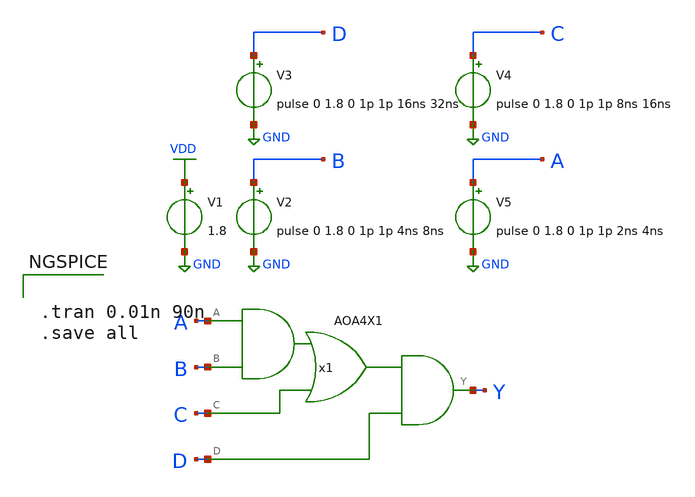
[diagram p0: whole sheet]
** sch_path: current/xschem/test_AOA4X1.sch
**.subckt test_AOA4X1
V2 B GND pulse 0 1.8 0 1p 1p 4ns 8ns
V1 VDD GND 1.8
V3 D GND pulse 0 1.8 0 1p 1p 16ns 32ns
V4 C GND pulse 0 1.8 0 1p 1p 8ns 16ns
V5 A GND pulse 0 1.8 0 1p 1p 2ns 4ns
x1 Y A B C D VDD GND AOA4X1
**** begin user architecture code

.lib $::SKYWATER_MODELS/sky130.lib.spice tt


**** end user architecture code
**.ends
.GLOBAL VDD
.GLOBAL GND
**** begin user architecture code


.tran 0.01n 90n
.save all


**** end user architecture code
.end
